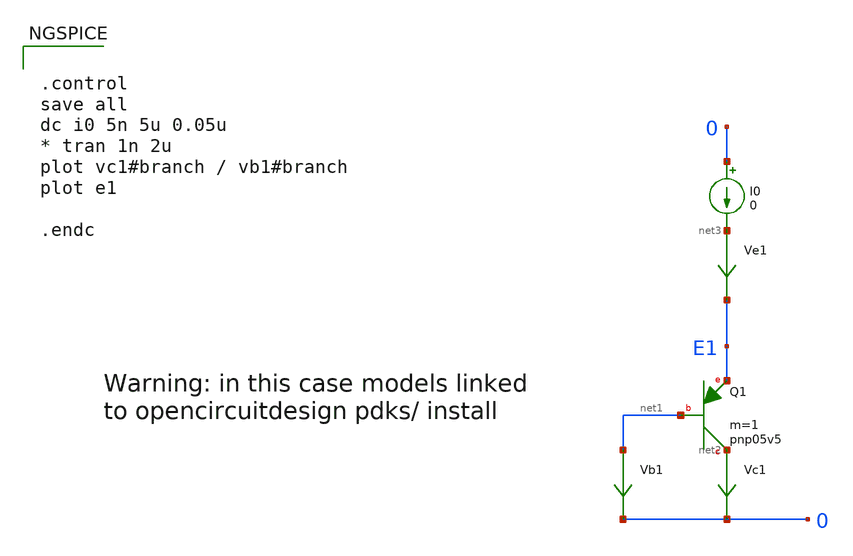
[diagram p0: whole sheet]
** sch_path: sky130_tests/test_bipolar.sch
* Copyright 2020 Stefan Frederik Schippers
* Licensed under the Apache License, Version 2.0 (the "License");
* you may not use this file except in compliance with the License.
* You may obtain a copy of the License at
* https://www.apache.org/licenses/LICENSE-2.0
* Unless required by applicable law or agreed to in writing, software
* distributed under the License is distributed on an "AS IS" BASIS,
* WITHOUT WARRANTIES OR CONDITIONS OF ANY KIND, either express or implied.
* See the License for the specific language governing permissions and
* limitations under the License.
**.subckt test_bipolar
XQ1 net2 net1 E1 sky130_fd_pr__pnp_05v5_W3p40L3p40 m=1
Vc1 net2 0 0
.save i(vc1)
Vb1 net1 0 0
.save i(vb1)
I0 0 net3 0
Ve1 net3 E1 0
.save i(ve1)
**** begin user architecture code


.control
save all
dc i0 5n 5u 0.05u
* tran 1n 2u
plot vc1#branch / vb1#branch
plot e1

.endc


 ** manual skywater pdks install (with patches applied)
* .lib $::SKYWATER_MODELS/models/sky130.lib.spice tt

** opencircuitdesign pdks install
.lib $::SKYWATER_MODELS/sky130.lib.spice tt

** manual skywater-pdk install (with patches applied).
* .include $::SKYWATER_MODELS/cells/pnp_05v5/sky130_fd_pr__pnp_05v5_W3p40L3p40.model.spice

** opencircuitdesign pdks install
.include $::SKYWATER_MODELS/../../libs.ref/sky130_fd_pr/spice/sky130_fd_pr__pnp_05v5_W3p40L3p40.model.spice

.param mc_mm_switch=0
.param mc_pr_switch=1

**** end user architecture code
**.ends
.end
